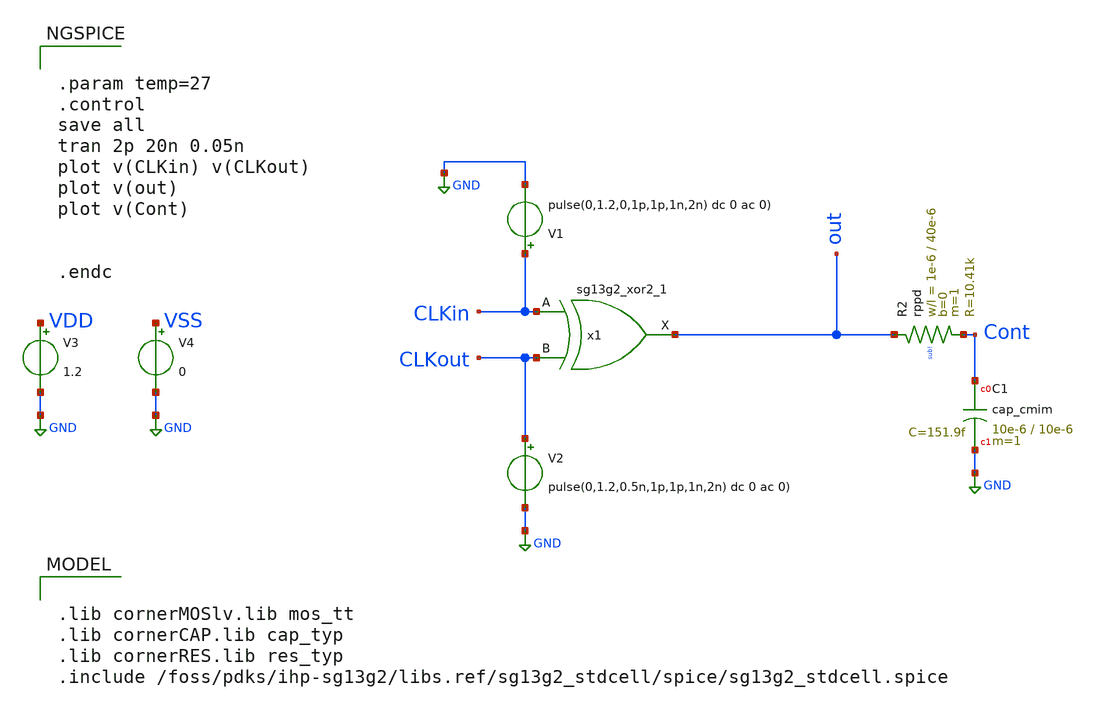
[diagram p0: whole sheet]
** sch_path: others/maxi/Simulacion_XOR.sch
**.subckt Simulacion_XOR
V1 CLKin GND pulse(0,1.2,0,1p,1p,1n,2n) dc 0 ac 0)
V2 CLKout GND pulse(0,1.2,0.5n,1p,1p,1n,2n) dc 0 ac 0)
x1 out CLKin CLKout VDD VSS sg13g2_xor2_1
V3 VDD GND 1.2
V4 VSS GND 0
XC1 Cont GND cap_cmim w=10e-6 l=10e-6 m=1 mm_ok=1
XR2 out Cont sub! rppd w=1e-6 l=40e-6 m=1 b=0 mm_ok=1
**** begin user architecture code

.lib cornerMOSlv.lib mos_tt
.lib cornerCAP.lib cap_typ
.lib cornerRES.lib res_typ
.include /foss/pdks/ihp-sg13g2/libs.ref/sg13g2_stdcell/spice/sg13g2_stdcell.spice



.param temp=27
.control
save all
tran 2p 20n 0.05n
plot v(CLKin) v(CLKout)
plot v(out)
plot v(Cont)


.endc


**** end user architecture code
**.ends

* expanding   symbol:  sg13g2_stdcells/sg13g2_xor2_1.sym # of pins=3
** sym_path: sg13g2_stdcells/sg13g2_xor2_1.sym
** sch_path: sg13g2_stdcells/sg13g2_xor2_1.sch
.subckt sg13g2_xor2_1 X A B VDD VSS
*.opin X
*.ipin B
*.ipin A
*.iopin VDD
*.iopin VSS
XM1 net1 A VSS VSS sg13_lv_nmos w=550.00n l=130.00n ng=1 m=1 mm_ok=1
XM2 net1 B VSS VSS sg13_lv_nmos w=550.00n l=130.00n ng=1 m=1 mm_ok=1
XM3 X net1 VSS VSS sg13_lv_nmos w=740.00n l=130.00n ng=1 m=1 mm_ok=1
XM4 X B net3 VSS sg13_lv_nmos w=740.00n l=130.00n ng=1 m=1 mm_ok=1
XM5 net3 A VSS VSS sg13_lv_nmos w=740.00n l=130.00n ng=1 m=1 mm_ok=1
XM6 net4 A VDD VDD sg13_lv_pmos w=1.000u l=130.00n ng=1 m=1 mm_ok=1
XM7 net1 B net4 VDD sg13_lv_pmos w=1.000u l=130.00n ng=1 m=1 mm_ok=1
XM8 net2 A VDD VDD sg13_lv_pmos w=1.12u l=130.00n ng=1 m=1 mm_ok=1
XM9 X net1 net2 VDD sg13_lv_pmos w=1.12u l=130.00n ng=1 m=1 mm_ok=1
XM10 net2 B VDD VDD sg13_lv_pmos w=1.12u l=130.00n ng=1 m=1 mm_ok=1
.ends

.GLOBAL GND
.end
